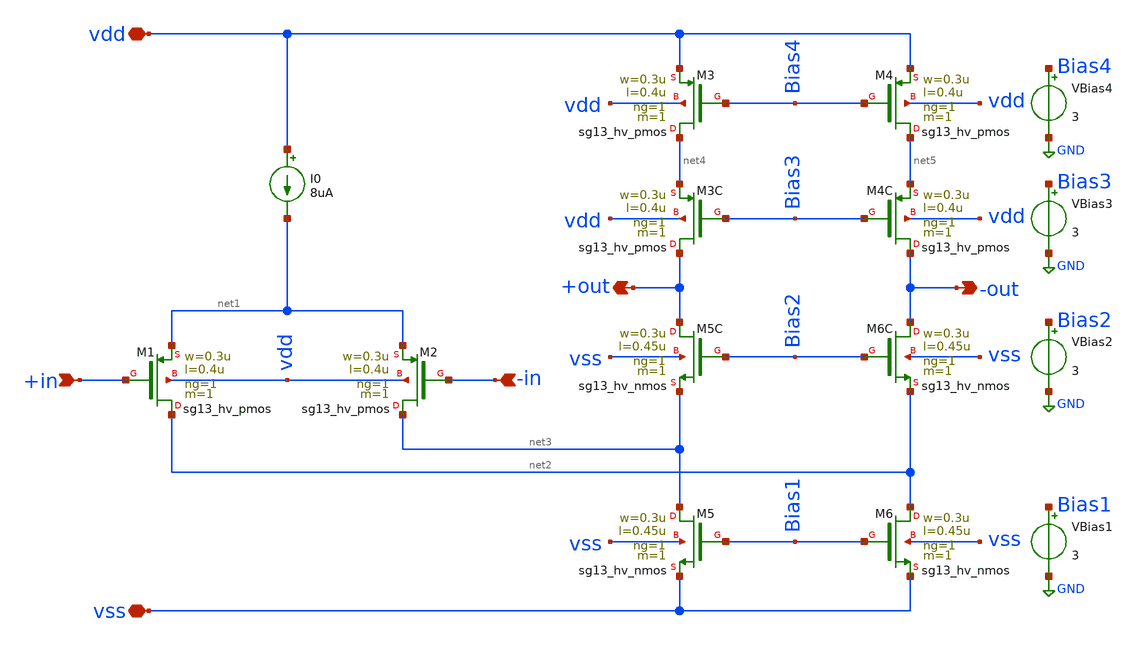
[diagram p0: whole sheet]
** sch_path: real_circuit/sandbox/cascaded_OTA.sch
**.subckt cascaded_OTA vdd vss +in -in -out +out
*.iopin vdd
*.iopin vss
*.ipin +in
*.ipin -in
*.opin -out
*.opin +out
I0 vdd net1 8uA
XM1 net2 +in net1 vdd sg13_hv_pmos w=0.3u l=0.4u ng=1 m=1 mm_ok=1
XM2 net3 -in net1 vdd sg13_hv_pmos w=0.3u l=0.4u ng=1 m=1 mm_ok=1
XM3 net4 Bias4 vdd vdd sg13_hv_pmos w=0.3u l=0.4u ng=1 m=1 mm_ok=1
XM4 net5 Bias4 vdd vdd sg13_hv_pmos w=0.3u l=0.4u ng=1 m=1 mm_ok=1
XM3C +out Bias3 net4 vdd sg13_hv_pmos w=0.3u l=0.4u ng=1 m=1 mm_ok=1
XM4C -out Bias3 net5 vdd sg13_hv_pmos w=0.3u l=0.4u ng=1 m=1 mm_ok=1
XM5C +out Bias2 net3 vss sg13_hv_nmos w=0.3u l=0.45u ng=1 m=1 mm_ok=1
XM6C -out Bias2 net2 vss sg13_hv_nmos w=0.3u l=0.45u ng=1 m=1 mm_ok=1
XM5 net3 Bias1 vss vss sg13_hv_nmos w=0.3u l=0.45u ng=1 m=1 mm_ok=1
XM6 net2 Bias1 vss vss sg13_hv_nmos w=0.3u l=0.45u ng=1 m=1 mm_ok=1
VBias4 Bias4 GND 3
VBias3 Bias3 GND 3
VBias2 Bias2 GND 3
VBias1 Bias1 GND 3
**.ends
.GLOBAL GND
.end
